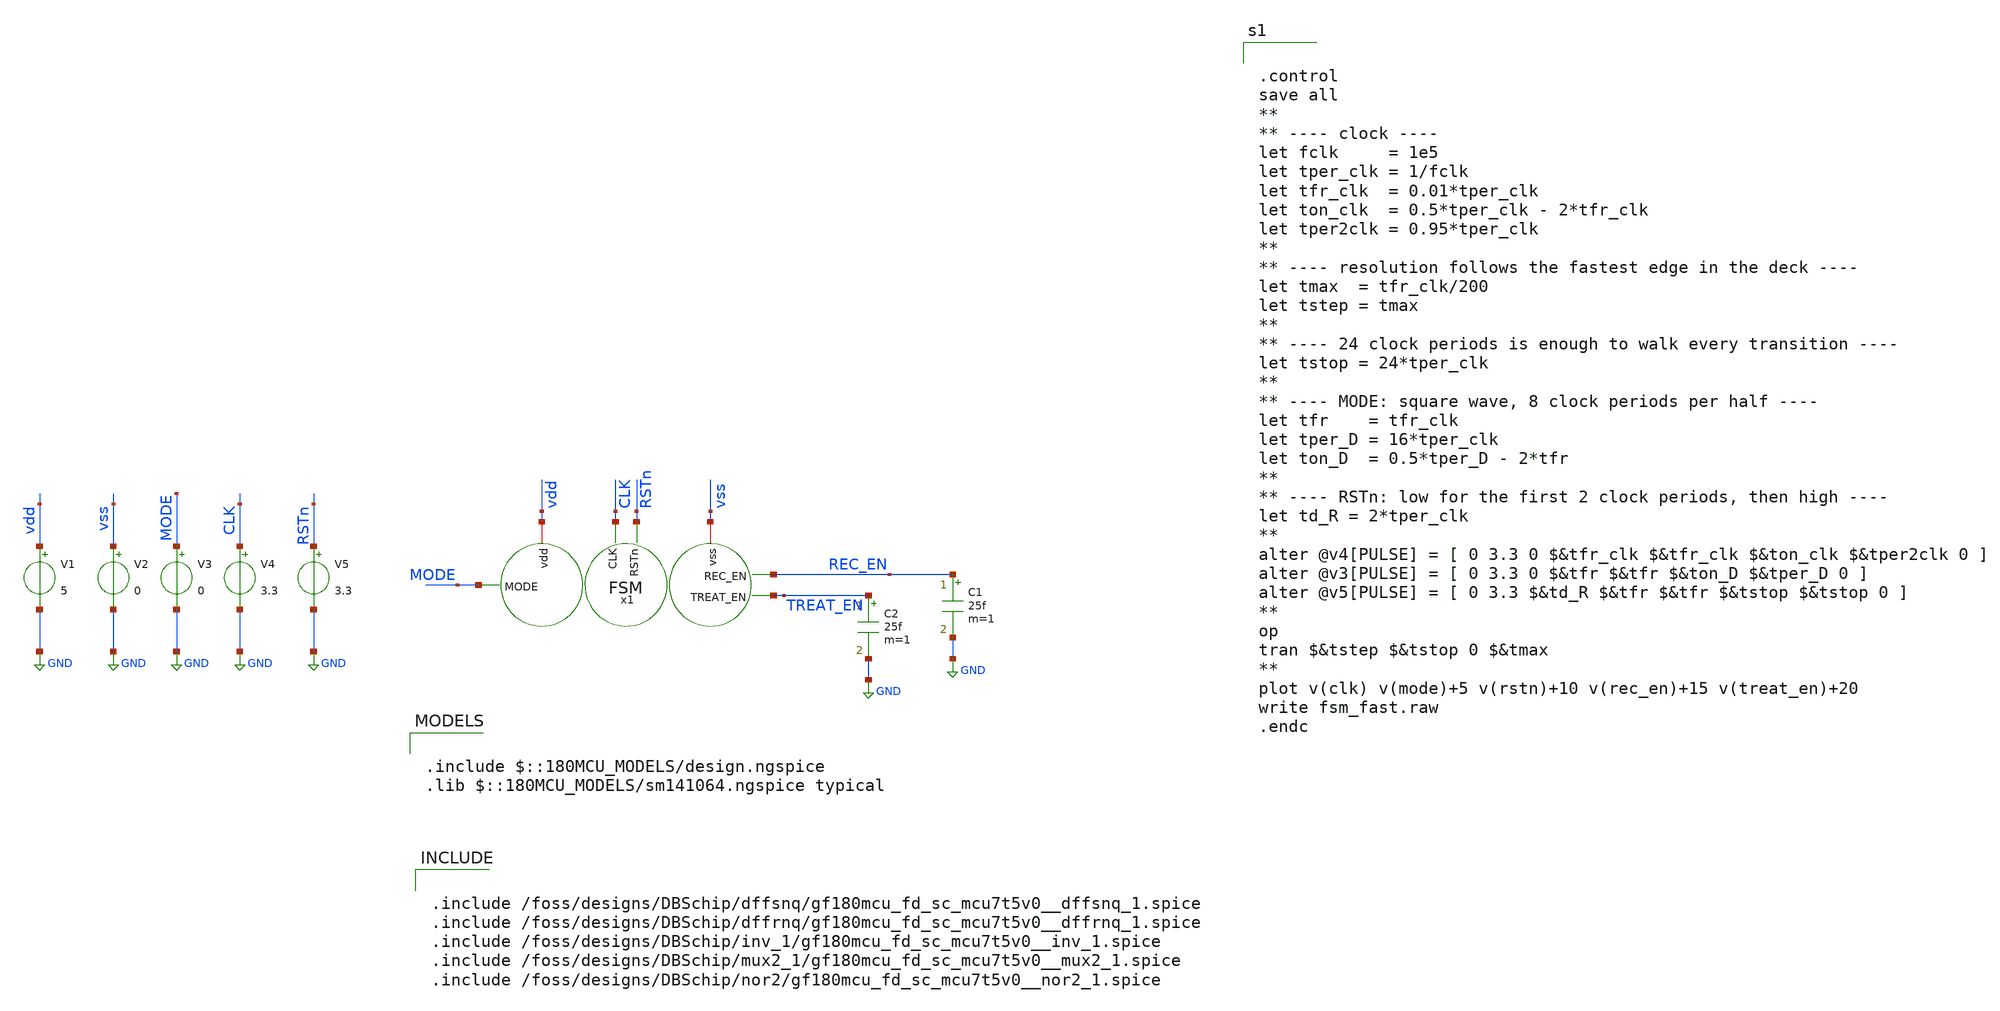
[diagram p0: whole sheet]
** sch_path: FSM/FSM_tb.sch
**.subckt FSM_tb
V1 vdd GND 5
V2 vss GND 0
V3 MODE GND 0
V4 CLK GND 3.3
V5 RSTn GND 3.3
C1 REC_EN GND 25f m=1
C2 TREAT_EN GND 25f m=1
x1 REC_EN TREAT_EN MODE RSTn CLK vdd vss FSM
**** begin user architecture code

.include $::180MCU_MODELS/design.ngspice
.lib $::180MCU_MODELS/sm141064.ngspice typical



.include /foss/designs/DBSchip/dffsnq/gf180mcu_fd_sc_mcu7t5v0__dffsnq_1.spice
.include /foss/designs/DBSchip/dffrnq/gf180mcu_fd_sc_mcu7t5v0__dffrnq_1.spice
.include /foss/designs/DBSchip/inv_1/gf180mcu_fd_sc_mcu7t5v0__inv_1.spice
.include /foss/designs/DBSchip/mux2_1/gf180mcu_fd_sc_mcu7t5v0__mux2_1.spice
.include /foss/designs/DBSchip/nor2/gf180mcu_fd_sc_mcu7t5v0__nor2_1.spice




.control
save all
**
** ---- clock ----
let fclk     = 1e5
let tper_clk = 1/fclk
let tfr_clk  = 0.01*tper_clk
let ton_clk  = 0.5*tper_clk - 2*tfr_clk
let tper2clk = 0.95*tper_clk
**
** ---- resolution follows the fastest edge in the deck ----
let tmax  = tfr_clk/200
let tstep = tmax
**
** ---- 24 clock periods is enough to walk every transition ----
let tstop = 24*tper_clk
**
** ---- MODE: square wave, 8 clock periods per half ----
let tfr    = tfr_clk
let tper_D = 16*tper_clk
let ton_D  = 0.5*tper_D - 2*tfr
**
** ---- RSTn: low for the first 2 clock periods, then high ----
let td_R = 2*tper_clk
**
alter @v4[PULSE] = [ 0 3.3 0 $&tfr_clk $&tfr_clk $&ton_clk $&tper2clk 0 ]
alter @v3[PULSE] = [ 0 3.3 0 $&tfr $&tfr $&ton_D $&tper_D 0 ]
alter @v5[PULSE] = [ 0 3.3 $&td_R $&tfr $&tfr $&tstop $&tstop 0 ]
**
op
tran $&tstep $&tstop 0 $&tmax
**
plot v(clk) v(mode)+5 v(rstn)+10 v(rec_en)+15 v(treat_en)+20
write fsm_fast.raw
.endc





**** end user architecture code
**.ends

* expanding   symbol:  FSM/FSM.sym # of pins=7
** sym_path: FSM/FSM.sym
** sch_path: FSM/FSM.sch
.subckt FSM REC_EN TREAT_EN MODE RSTn CLK vdd vss
*.opin REC_EN
*.ipin MODE
*.ipin RSTn
*.ipin CLK
*.opin TREAT_EN
*.iopin vdd
*.iopin vss
x1 REC_EN S0 TREAT_EN vdd vdd vss vss gf180mcu_fd_sc_mcu7t5v0__nor2_1
x2 TREAT_EN net1 net3 vdd vdd vss vss gf180mcu_fd_sc_mcu7t5v0__nor2_1
x3 MODE net1 vdd vdd vss vss gf180mcu_fd_sc_mcu7t5v0__inv_1
x4 REC_EN TREAT_EN MODE net2 vdd vdd vss vss gf180mcu_fd_sc_mcu7t5v0__mux2_1
x5 net3 RSTn CLK REC_EN vdd vdd vss vss gf180mcu_fd_sc_mcu7t5v0__dffrnq_1
x6 net2 RSTn CLK S0 vdd vdd vss vss gf180mcu_fd_sc_mcu7t5v0__dffsnq_1
.ends

.GLOBAL GND
.end
